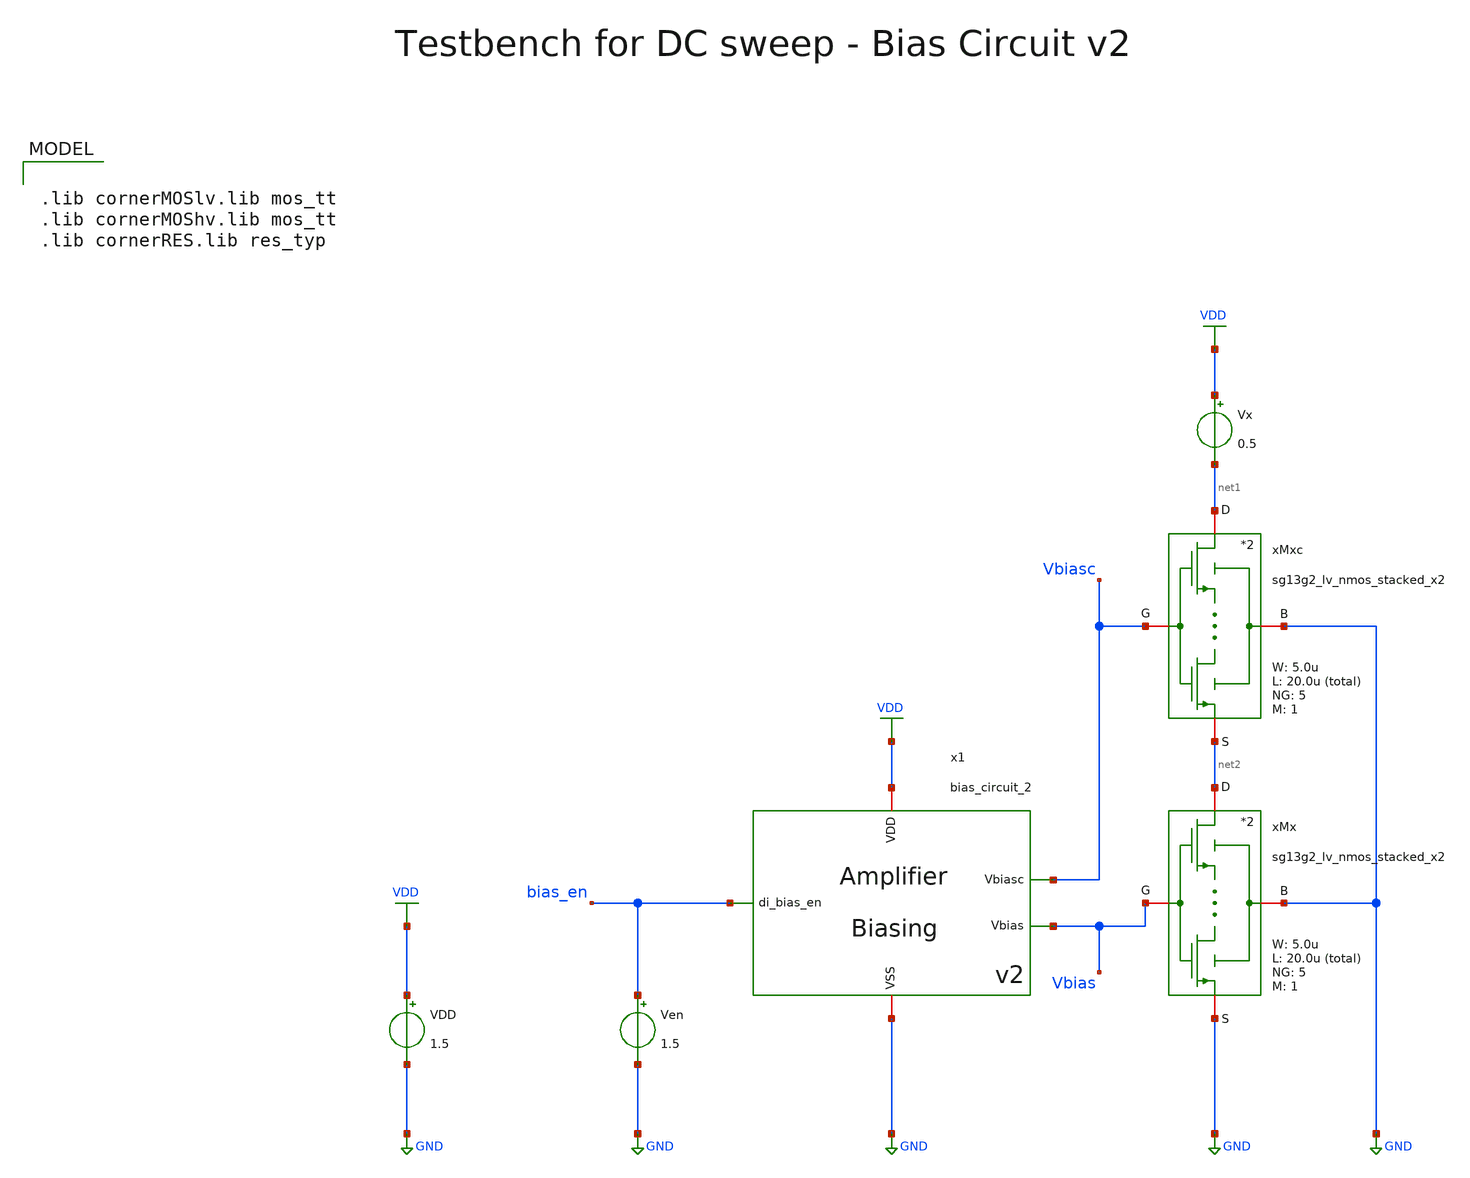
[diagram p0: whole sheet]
** sch_path: SG13G2_ATBS-ADC-main/xschem/bio_amplifier/amplifier_core/bias_circuit/bias_circuit_2/testbenches/bias_circuit_2_tb_dc.sch
**.subckt bias_circuit_2_tb_dc
Ven bias_en GND 1.5
VDD VDD GND 1.5
Vx VDD net1 0.5
x1 bias_en Vbiasc VDD GND Vbias bias_circuit_2
xMx net2 Vbias GND GND sg13g2_lv_nmos_stacked_x2 W_N=5.0u L_N=20.0u NG_N=5 M_N=1
xMxc net1 Vbiasc GND net2 sg13g2_lv_nmos_stacked_x2 W_N=5.0u L_N=20.0u NG_N=5 M_N=1
**** begin user architecture code

.lib cornerMOSlv.lib mos_tt
.lib cornerMOShv.lib mos_tt
.lib cornerRES.lib res_typ



.param temp=27
.options savecurrents reltol=1e-3 abstol=1e-15 gmin=1e-15
.control

save all

* Operating Point Analysis
op
remzerovec
write bias_circuit_2_tb_dc.raw
set appendwrite

* DC Sweep of Vout
dc Vx 0 1.5 5m
remzerovec
write bias_circuit_2_tb_dc.raw

* Plotting
plot i(Vx) xlabel Vx

* Measurements
meas dc Ix_1V FIND i(Vx) at=1
meas dc Ix_0V FIND i(Vx) at=0
let Ix_volt = Ix_0V - Ix_1V
print Ix_volt

* DC Sweep of VDD
dc VDD 0 1.5 5m
remzerovec
write bias_circuit_2_tb_dc.raw

* Plotting
plot v(Vbiasc) v(Vbias) xlabel VDD
plot i(Vx) xlabel VDD
plot i(v.x1.viref) i(v.x1.viout) xlabel VDD

* Measurements
let Iout_nominal = 10e-9
let Iout_99_percent = 0.99 * Iout_nominal
print Iout_99_percent
meas dc VDD_min WHEN i(v.x1.viout)=Iout_99_percent

meas dc Iout_1_4V FIND i(v.x1.viout) at=1.4
meas dc Iout_1_3V FIND i(v.x1.viout) at=1.3
let Iout_volt = (Iout_1_4V - Iout_1_3V) * 10
print Iout_volt

* Write Data
set wr_vecnames
set wr_singlescale
let Ix=i(Vx)
let Iout=i(v.x1.viout)
let Iref=i(v.x1.viref)
wrdata /foss/designs/SG13G2_ATBS-ADC-main/python/plot_simulations/data/bias_circuit_2_tb_dc.txt
+ v(Vbiasc) v(Vbias) v(Ix) v(Iout) v(Iref)

*quit
.endc

**** end user architecture code
**.ends

* expanding   symbol:  bio_amplifier/amplifier_core/bias_circuit/bias_circuit_2/bias_circuit_2.sym #
*+ of pins=5
** sym_path: SG13G2_ATBS-ADC-main/xschem/bio_amplifier/amplifier_core/bias_circuit/bias_circuit_2/bias_circuit_2.sym
** sch_path: SG13G2_ATBS-ADC-main/xschem/bio_amplifier/amplifier_core/bias_circuit/bias_circuit_2/bias_circuit_2.sch
.subckt bias_circuit_2 di_bias_en Vbiasc VDD VSS Vbias
*.iopin VDD
*.iopin VSS
*.opin Vbias
*.ipin di_bias_en
*.opin Vbiasc
R1 net3 VSS 3.72Meg m=1
XMDEC1 net1 Vbias net1 net1 sg13_lv_nmos w=100.0u l=40.0u ng=100 m=1 mm_ok=1
VIref net4 net8 0
.save i(viref)
VIout net9 Vbiasc 0
.save i(viout)
x1 VDD di_bias_en bias_en_n VSS inverter_lv W_P=1.0u L_P=0.13u W_N=1.0u L_N=0.13u
xMSU2 Vsu net6 VSS VSS sg13g2_lv_nmos_stacked_x4 W_N=1.0u L_N=40.0u NG_N=1 M_N=1
xMSU1 net5 Vsu VSS net6 sg13g2_lv_nmos_stacked_x4 W_N=1.0u L_N=40.0u NG_N=1 M_N=1
Vmeas1 net4 net5 0
.save i(vmeas1)
Vmeas2 Vbias net6 0
.save i(vmeas2)
XMPD1 Vgs_m34 di_bias_en net2 net2 sg13_lv_pmos w=1.0u l=0.13u ng=1 m=1 mm_ok=1
XMPD2 net4 bias_en_n Vgs_m34 net2 sg13_lv_pmos w=1.0u l=0.13u ng=1 m=1 mm_ok=1
XMPD3 Vbias bias_en_n VSS VSS sg13_lv_nmos w=1.0u l=0.13u ng=1 m=1 mm_ok=1
VIref5 net1 VSS 0
.save i(viref5)
VIdd VDD net2 0
.save i(vidd)
CSU1 net10 Vsu 35f m=1
xM1 net7 Vbias VSS net3 sg13g2_lv_nmos_stacked_x2 W_N=20.0u L_N=20.0u NG_N=20 M_N=1
xM1c net8 Vbiasc VSS net7 sg13g2_lv_nmos_stacked_x2 W_N=5.0u L_N=20.0u NG_N=5 M_N=1
xM2 Vbias Vbias VSS VSS sg13g2_lv_nmos_stacked_x2 W_N=5.0u L_N=20.0u NG_N=5 M_N=1
xM2c Vbiasc Vbiasc VSS Vbias sg13g2_lv_nmos_stacked_x2 W_N=5.0u L_N=20.0u NG_N=5 M_N=1
XMDEC2 net2 Vgs_m34 net2 net2 sg13_lv_pmos w=25.0u l=40.0u ng=25 m=1 mm_ok=1
xM3 net4 Vgs_m34 net2 net2 sg13g2_lv_pmos_stacked_x4 W_P=20.0u L_P=40.0u NG_P=20 M_P=1
xM4 net9 Vgs_m34 net2 net2 sg13g2_lv_pmos_stacked_x4 W_P=20.0u L_P=40.0u NG_P=20 M_P=1
XMPD6 Vsu di_bias_en net10 net10 sg13_lv_pmos w=1.0u l=0.13u ng=1 m=1 mm_ok=1
XMPD4 Vbiasc bias_en_n VSS VSS sg13_lv_nmos w=1.0u l=0.13u ng=1 m=1 mm_ok=1
XMPD7 Vsu bias_en_n VSS VSS sg13_lv_nmos w=1.0u l=0.13u ng=1 m=1 mm_ok=1
XMPD5 net10 bias_en_n net2 net2 sg13_lv_pmos w=1.0u l=0.13u ng=1 m=1 mm_ok=1
.ends


* expanding   symbol:  stacked_transistors/sg13g2_lv_nmos_stacked/sg13g2_lv_nmos_stacked_x2.sym # of
*+ pins=4
** sym_path: SG13G2_ATBS-ADC-main/xschem/stacked_transistors/sg13g2_lv_nmos_stacked/sg13g2_lv_nmos_stacked_x2.sym
** sch_path: SG13G2_ATBS-ADC-main/xschem/stacked_transistors/sg13g2_lv_nmos_stacked/sg13g2_lv_nmos_stacked_x2.sch
.subckt sg13g2_lv_nmos_stacked_x2 D G B S  W_N=1.0u L_N=0.45u NG_N=1 M_N=1
*.iopin D
*.iopin S
*.iopin G
*.iopin B
XM1 net1 G S B sg13_lv_nmos w=W_N l=L_N/2 ng=NG_N m=M_N mm_ok=1
XM2 D G net1 B sg13_lv_nmos w=W_N l=L_N/2 ng=NG_N m=M_N mm_ok=1
.ends


* expanding   symbol:  inverter/inverter_lv.sym # of pins=4
** sym_path: SG13G2_ATBS-ADC-main/xschem/inverter/inverter_lv.sym
** sch_path: SG13G2_ATBS-ADC-main/xschem/inverter/inverter_lv.sch
.subckt inverter_lv VDD vin vout VSS  W_P=3.0u L_P=0.13u W_N=1.0u L_N=0.13u
*.ipin vin
*.iopin VDD
*.iopin VSS
*.opin vout
XM1 vout vin VDD VDD sg13_lv_pmos w=W_P l=L_P ng=1 m=1 mm_ok=1
XM2 vout vin VSS VSS sg13_lv_nmos w=W_N l=L_N ng=1 m=1 mm_ok=1
.ends


* expanding   symbol:  stacked_transistors/sg13g2_lv_nmos_stacked/sg13g2_lv_nmos_stacked_x4.sym # of
*+ pins=4
** sym_path: SG13G2_ATBS-ADC-main/xschem/stacked_transistors/sg13g2_lv_nmos_stacked/sg13g2_lv_nmos_stacked_x4.sym
** sch_path: SG13G2_ATBS-ADC-main/xschem/stacked_transistors/sg13g2_lv_nmos_stacked/sg13g2_lv_nmos_stacked_x4.sch
.subckt sg13g2_lv_nmos_stacked_x4 D G B S  W_N=1.0u L_N=0.45u NG_N=1 M_N=1
*.iopin D
*.iopin S
*.iopin G
*.iopin B
XM1 net1 G S B sg13_lv_nmos w=W_N l=L_N/4 ng=NG_N m=M_N mm_ok=1
XM2 net3 G net1 B sg13_lv_nmos w=W_N l=L_N/4 ng=NG_N m=M_N mm_ok=1
XM3 net2 G net3 B sg13_lv_nmos w=W_N l=L_N/4 ng=NG_N m=M_N mm_ok=1
XM4 D G net2 B sg13_lv_nmos w=W_N l=L_N/4 ng=NG_N m=M_N mm_ok=1
.ends


* expanding   symbol:  stacked_transistors/sg13g2_lv_pmos_stacked/sg13g2_lv_pmos_stacked_x4.sym # of
*+ pins=4
** sym_path: SG13G2_ATBS-ADC-main/xschem/stacked_transistors/sg13g2_lv_pmos_stacked/sg13g2_lv_pmos_stacked_x4.sym
** sch_path: SG13G2_ATBS-ADC-main/xschem/stacked_transistors/sg13g2_lv_pmos_stacked/sg13g2_lv_pmos_stacked_x4.sch
.subckt sg13g2_lv_pmos_stacked_x4 D G B S  W_P=1.0u L_P=0.45u NG_P=1 M_P=1
*.iopin D
*.iopin S
*.iopin G
*.iopin B
XM1 net1 G S B sg13_lv_pmos w=W_P l=L_P/4 ng=NG_P m=M_P mm_ok=1
XM2 net3 G net1 B sg13_lv_pmos w=W_P l=L_P/4 ng=NG_P m=M_P mm_ok=1
XM3 net2 G net3 B sg13_lv_pmos w=W_P l=L_P/4 ng=NG_P m=M_P mm_ok=1
XM4 D G net2 B sg13_lv_pmos w=W_P l=L_P/4 ng=NG_P m=M_P mm_ok=1
.ends

.GLOBAL GND
.GLOBAL VDD
.end
